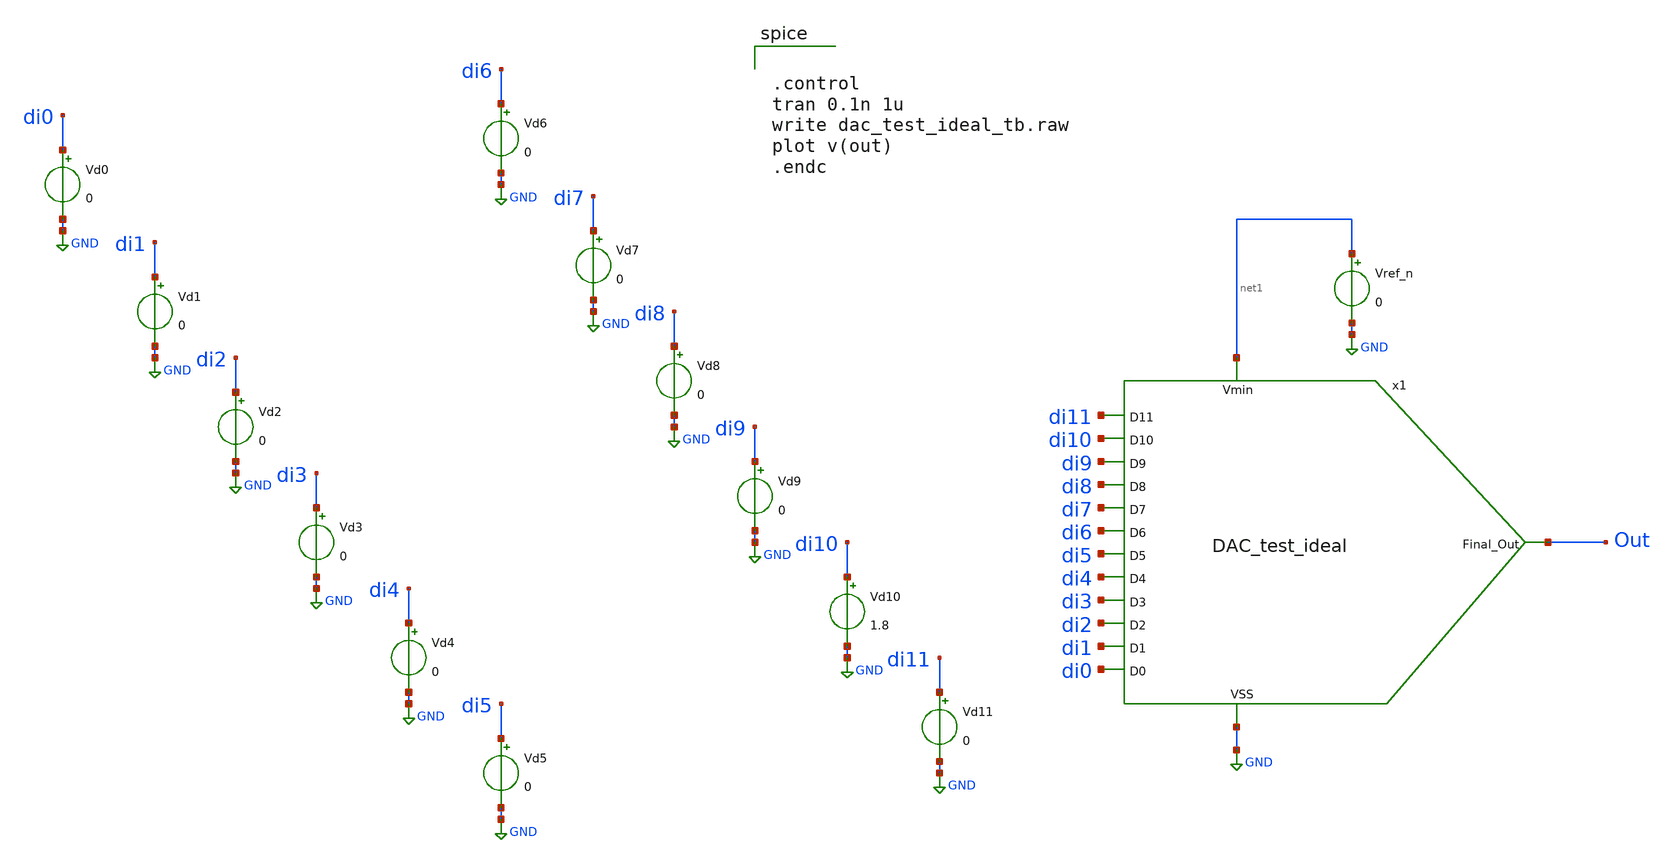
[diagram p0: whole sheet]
** sch_path: DAC_test_ideal_tb.sch
**.subckt DAC_test_ideal_tb
x1 Out GND net1 di7 di3 di11 di10 di6 di2 di5 di1 di9 di0 di4 di8 DAC_test_ideal
Vd0 di0 GND 0
Vd1 di1 GND 0
Vd2 di2 GND 0
Vd3 di3 GND 0
Vd4 di4 GND 0
Vd5 di5 GND 0
Vd6 di6 GND 0
Vd7 di7 GND 0
Vd8 di8 GND 0
Vd9 di9 GND 0
Vd10 di10 GND 1.8
Vd11 di11 GND 0
Vref_n net1 GND 0
**** begin user architecture code


.control
tran 0.1n 1u
write dac_test_ideal_tb.raw
plot v(out)
.endc


**** end user architecture code
**.ends

* expanding   symbol:  project/DAC_test_ideal.sym # of pins=15
** sym_path: DAC_test_ideal.sym
** sch_path: DAC_test_ideal.sch
.subckt DAC_test_ideal Final_Out VSS Vmin D7 D3 D11 D10 D6 D2 D5 D1 D9 D0 D4 D8
*.ipin D11
*.ipin D10
*.ipin D9
*.ipin D8
*.ipin D7
*.ipin D6
*.ipin D5
*.ipin D4
*.ipin D3
*.ipin D2
*.ipin D1
*.ipin D0
*.ipin Vmin
*.ipin VSS
*.opin Final_Out
E1 net12 net1 D11 VSS 0.5
E2 net1 net2 D10 VSS 0.25
E3 net2 net3 D9 VSS 0.125
E4 net3 net4 D8 VSS 0.0625
E5 net4 net5 D7 VSS 0.03125
E6 net5 net6 D6 VSS 0.015625
E7 net6 net7 D5 VSS 7.8125e-3
E8 net7 net8 D4 VSS 3.90625e-3
E9 net8 net9 D3 VSS 1.953125e-3
E10 net9 net10 D2 VSS 9.765625e-4
E11 net10 net11 D1 VSS 4.8828125e-4
E12 net11 VSS D0 VSS 2.44140625e-4
E13 Final_Out Vmin net12 VSS {gain}
.ends

.GLOBAL GND
.end
